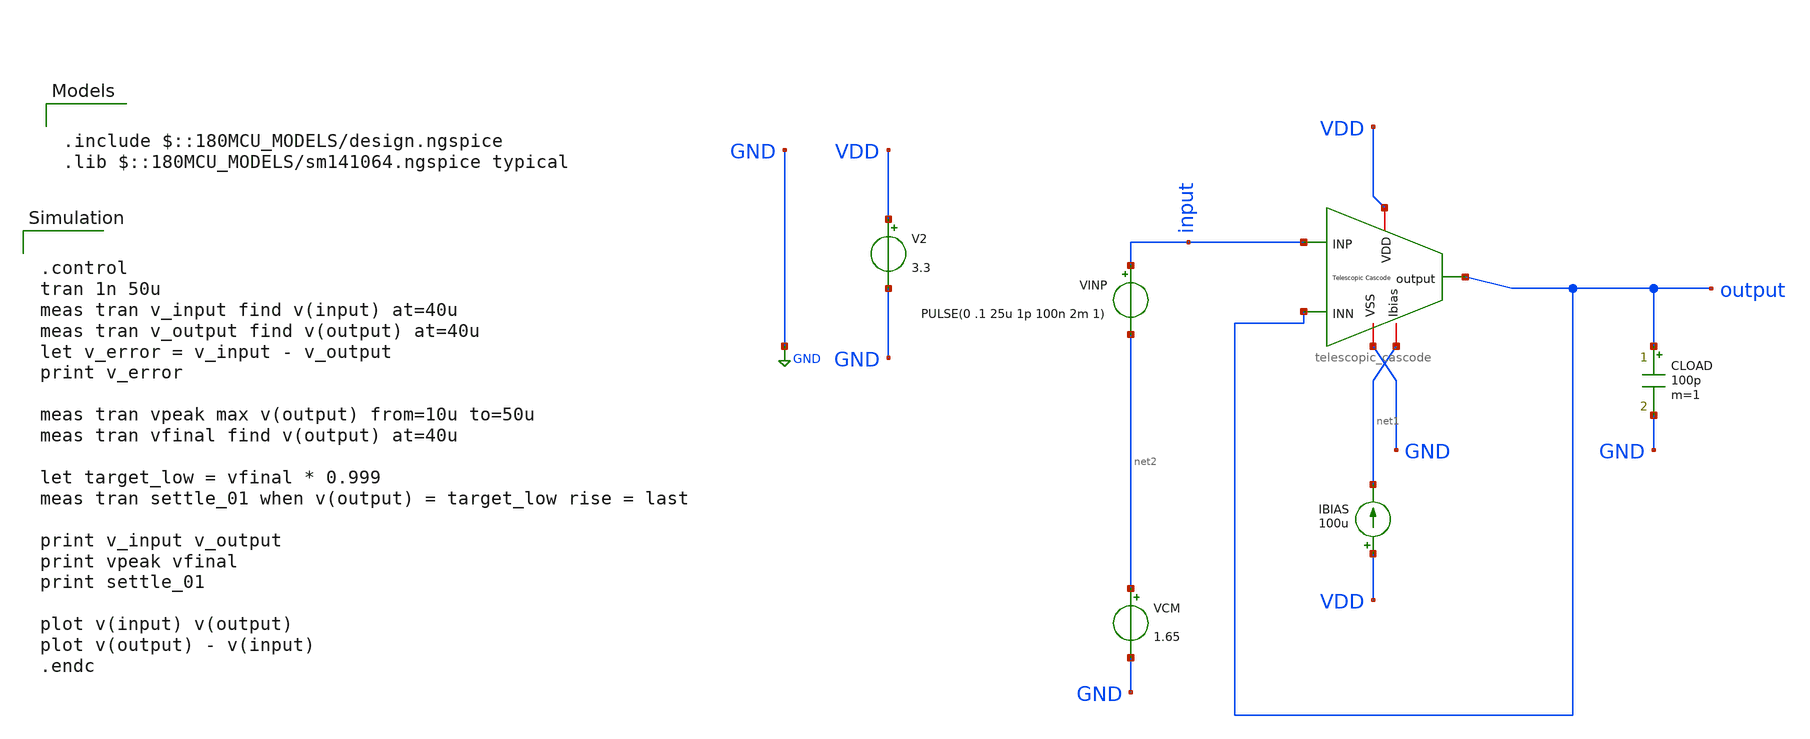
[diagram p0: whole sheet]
** sch_path: designs/libs/core_amps/ota_telescopic/tb/telescopic_small_step_settling_tb.sch
**.subckt telescopic_small_step_settling_tb
IBIAS VDD net1 100u
V2 VDD GND 3.3
CLOAD output GND 100p m=1
VINP input net2 PULSE(0 .1 25u 1p 100n 2m 1)
VCM net2 GND 1.65
x1 VDD output output input GND net1 telescopic_cascode
**** begin user architecture code

.include $::180MCU_MODELS/design.ngspice
.lib $::180MCU_MODELS/sm141064.ngspice typical



.control
tran 1n 50u
meas tran v_input find v(input) at=40u
meas tran v_output find v(output) at=40u
let v_error = v_input - v_output
print v_error

meas tran vpeak max v(output) from=10u to=50u
meas tran vfinal find v(output) at=40u

let target_low = vfinal * 0.999
meas tran settle_01 when v(output) = target_low rise = last

print v_input v_output
print vpeak vfinal
print settle_01

plot v(input) v(output)
plot v(output) - v(input)
.endc


**** end user architecture code
**.ends
.GLOBAL GND
.end
